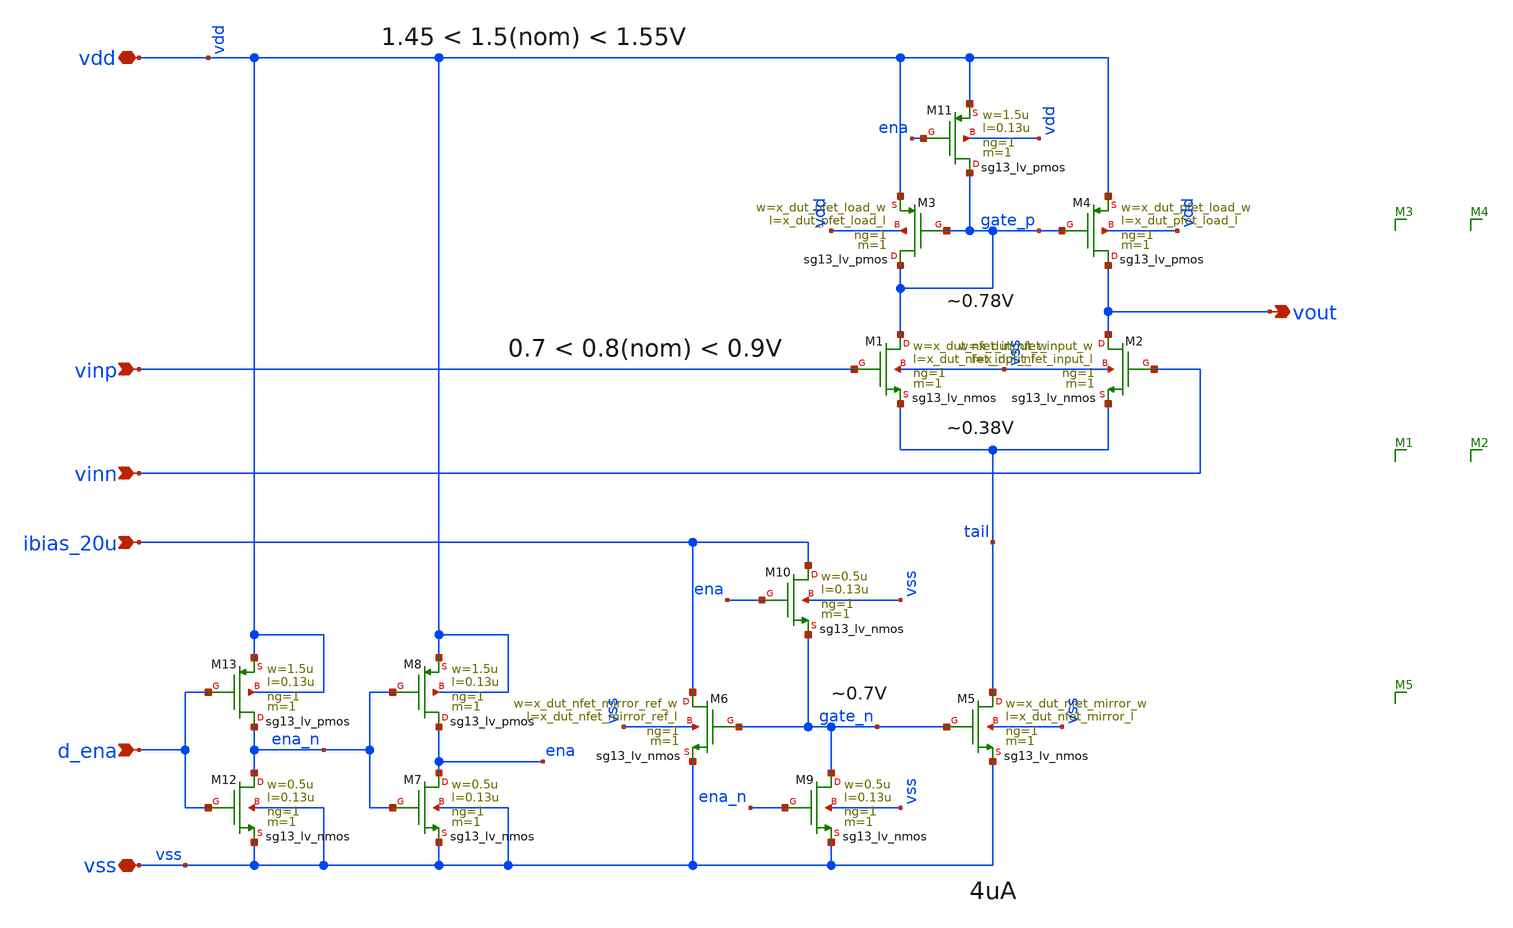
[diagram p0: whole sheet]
** sch_path: platform/examples/OTA/5t-ota/ihp-sg13g2/xschem/ota-5t.sch
* (c) 2024-2025 H. Pretl, Apache-2.0 license
**.subckt ota-5t ibias_20u vdd vss vinp vinn vout d_ena
*.ipin ibias_20u
*.iopin vdd
*.iopin vss
*.ipin vinp
*.ipin vinn
*.opin vout
*.ipin d_ena
XM5 tail gate_n vss vss sg13_lv_nmos w=x_dut_nfet_mirror_w l=x_dut_nfet_mirror_l ng=1 m=1 mm_ok=1
XM4 vout gate_p vdd vdd sg13_lv_pmos w=x_dut_pfet_load_w l=x_dut_pfet_load_l ng=1 m=1 mm_ok=1
XM1 gate_p vinp tail vss sg13_lv_nmos w=x_dut_nfet_input_w l=x_dut_nfet_input_l ng=1 m=1 mm_ok=1
XM2 vout vinn tail vss sg13_lv_nmos w=x_dut_nfet_input_w l=x_dut_nfet_input_l ng=1 m=1 mm_ok=1
XM3 gate_p gate_p vdd vdd sg13_lv_pmos w=x_dut_pfet_load_w l=x_dut_pfet_load_l ng=1 m=1 mm_ok=1
XM6 ibias_20u gate_n vss vss sg13_lv_nmos w=x_dut_nfet_mirror_ref_w l=x_dut_nfet_mirror_ref_l ng=1
+ m=1 mm_ok=1
XM9 gate_n ena_n vss vss sg13_lv_nmos w=0.5u l=0.13u ng=1 m=1 mm_ok=1
XM11 gate_p ena vdd vdd sg13_lv_pmos w=1.5u l=0.13u ng=1 m=1 mm_ok=1
XM7 ena ena_n vss vss sg13_lv_nmos w=0.5u l=0.13u ng=1 m=1 mm_ok=1
XM8 ena ena_n vdd vdd sg13_lv_pmos w=1.5u l=0.13u ng=1 m=1 mm_ok=1
XM10 ibias_20u ena gate_n vss sg13_lv_nmos w=0.5u l=0.13u ng=1 m=1 mm_ok=1
XM12 ena_n d_ena vss vss sg13_lv_nmos w=0.5u l=0.13u ng=1 m=1 mm_ok=1
XM13 ena_n d_ena vdd vdd sg13_lv_pmos w=1.5u l=0.13u ng=1 m=1 mm_ok=1
**.ends
.end
